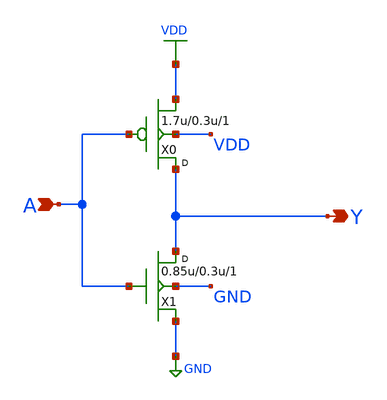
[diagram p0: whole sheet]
** sch_path: gf180mcu_osu_sc_gp12t3v3/cells/clkinv/gf180mcu_osu_sc_gp12t3v3__clkinv_1.sch
**.subckt gf180mcu_osu_sc_gp12t3v3__clkinv_1 A Y
*.ipin A
*.opin Y
X0 Y A VDD VDD pfet_03p3 w=1.7u l=0.3u m=1
X1 Y A GND GND nfet_03p3 w=0.85u l=0.3u m=1
**.ends
.GLOBAL VDD
.GLOBAL GND
.end
